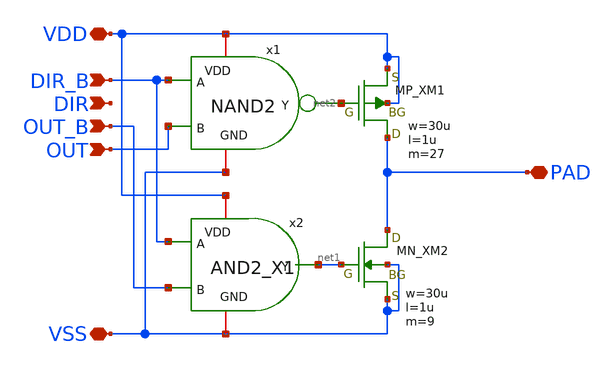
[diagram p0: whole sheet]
** sch_path: technology/tr1um_hand_support_v1/gpio_o.sch
**.subckt gpio_o VDD VSS DIR DIR_B OUT OUT_B PAD
*.iopin VDD
*.iopin VSS
*.ipin DIR
*.ipin DIR_B
*.ipin OUT
*.ipin OUT_B
*.iopin PAD
x1 VDD net2 DIR_B OUT VSS NAND2
XXM1 PAD net2 VDD VDD PMOS w=30u l=1u nrd=0 nrs=0 m=27
x2 VDD net1 DIR_B OUT_B VSS AND2_X1
XXM2 PAD net1 VSS VSS NMOS w=30u l=1u nrd=0 nrs=0 m=9
**.ends
.end
